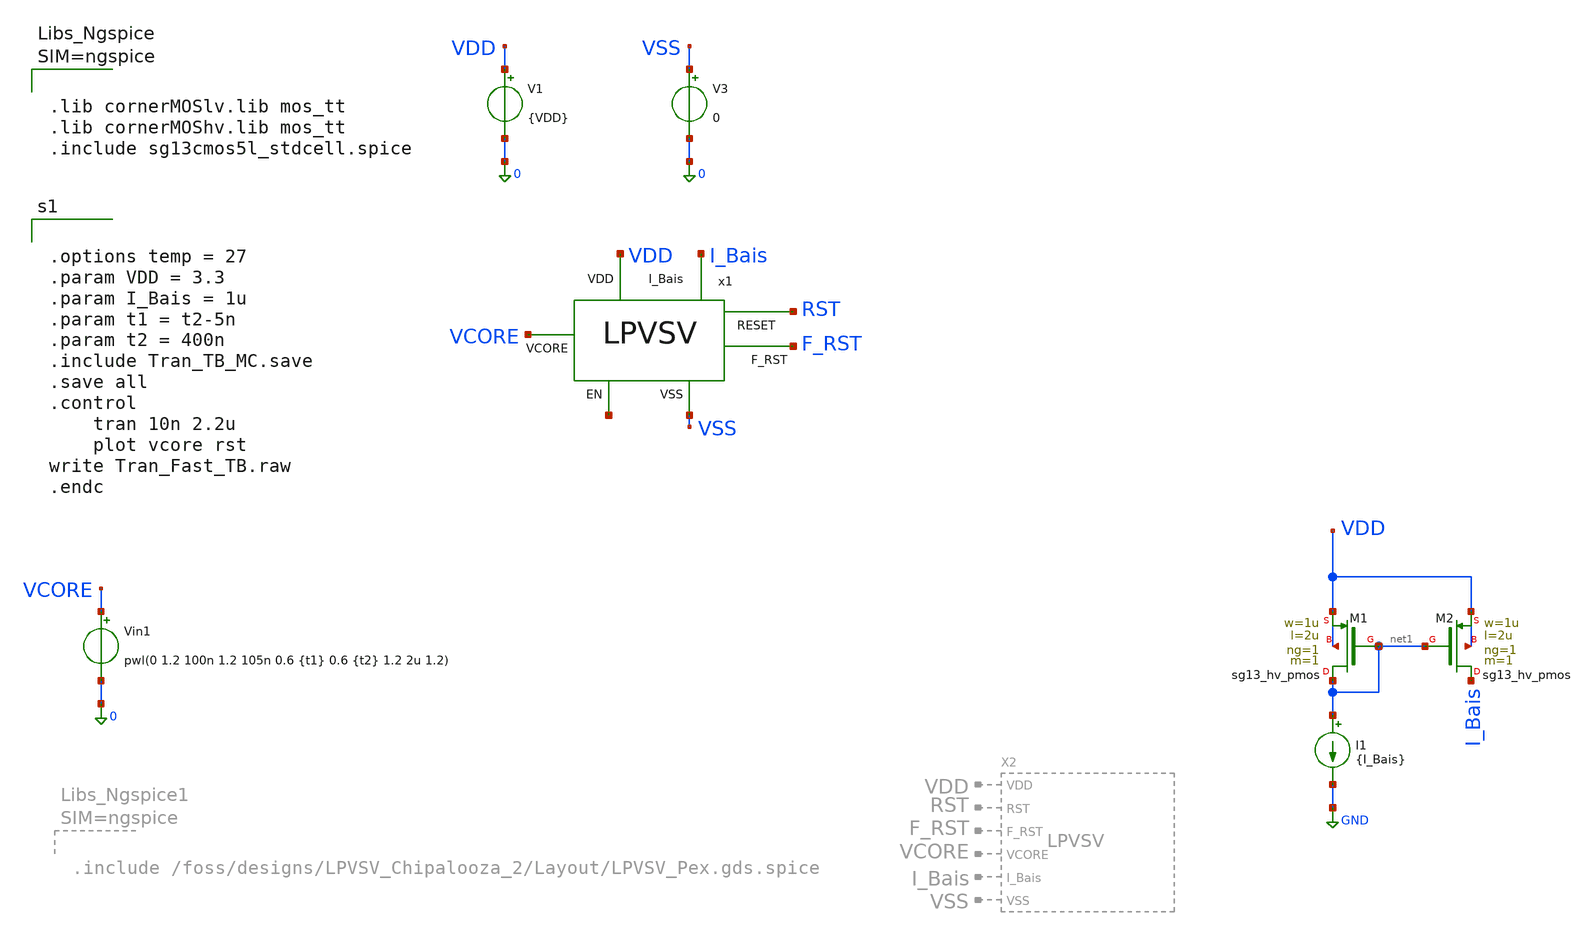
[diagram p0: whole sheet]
** sch_path: Simulation/Tran_Fast_TB.sch
**.subckt Tran_Fast_TB
V1 VDD 0 {VDD}
V3 VSS 0 0
x1 VDD VCORE I_Bais RST F_RST VSS net2 LPVSV
I1 net1 GND {I_Bais}
XM1 net1 net1 VDD VDD sg13_hv_pmos w=1u l=2u ng=1 m=1 mm_ok=1
XM2 I_Bais net1 VDD VDD sg13_hv_pmos w=1u l=2u ng=1 m=1 mm_ok=1
Vin1 VCORE 0 pwl(0 1.2 100n 1.2 105n 0.6 {t1} 0.6 {t2} 1.2 2u 1.2)
**** begin user architecture code



.lib cornerMOSlv.lib mos_tt
.lib cornerMOShv.lib mos_tt
.include sg13cmos5l_stdcell.spice





.options temp = 27
.param VDD = 3.3
.param I_Bais = 1u
.param t1 = t2-5n
.param t2 = 400n
.include Tran_TB_MC.save
.save all
.control
	tran 10n 2.2u
	plot vcore rst
write Tran_Fast_TB.raw
.endc


**** end user architecture code
**.ends
.GLOBAL GND
.end
